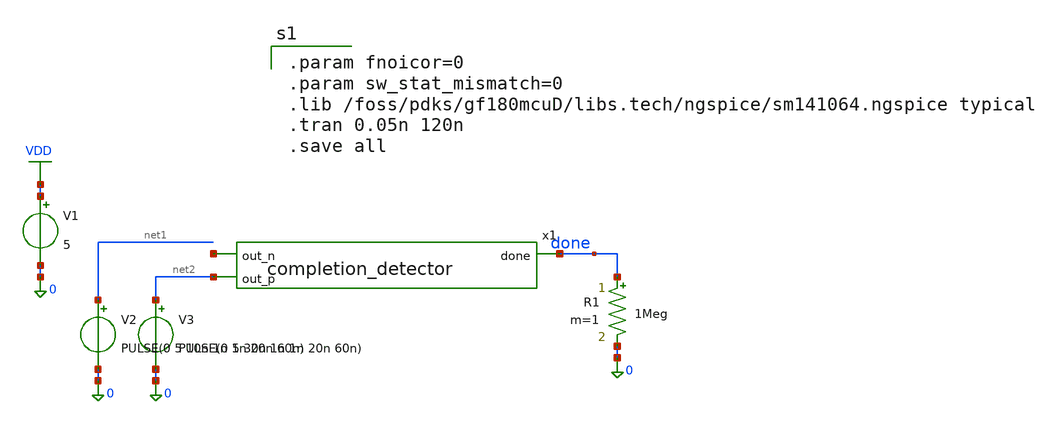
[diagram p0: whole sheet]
** sch_path: xschem/sar_adc/blocks/async_sar/testbench/tb_completion_detector.sch
**.subckt tb_completion_detector
x1 net3 net2 done completion_detector
V1 VDD 0 5
V2 net1 0 PULSE(0 5 10n 1n 1n 20n 60n)
V3 net2 0 PULSE(0 5 30n 1n 1n 20n 60n)
R1 done 0 1Meg m=1
**** begin user architecture code

.param fnoicor=0
.param sw_stat_mismatch=0
.lib /foss/pdks/gf180mcuD/libs.tech/ngspice/sm141064.ngspice typical
.tran 0.05n 120n
.save all

**** end user architecture code
**.ends
.GLOBAL VDD
.end
